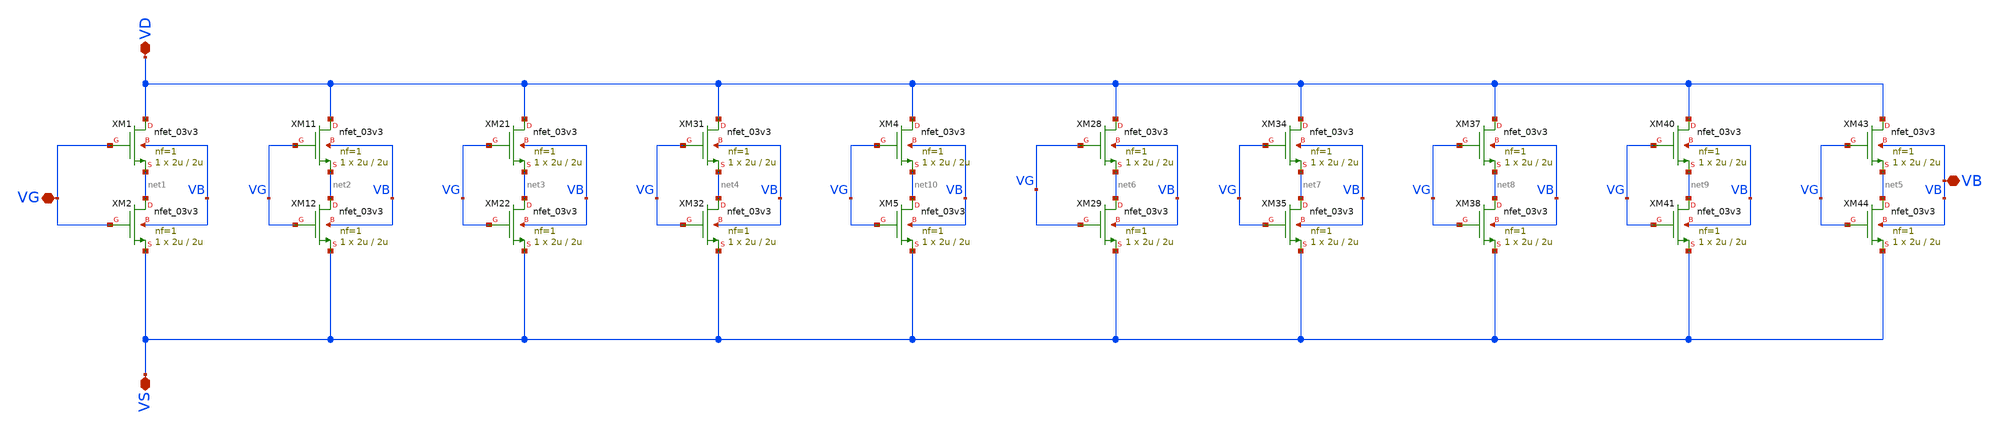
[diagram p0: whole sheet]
** sch_path: Voltage_Reference/symbols_vr/NMOS_association_10u_6u_V2.sch
**.subckt NMOS_association_10u_6u_V2 VD VB VG VS
*.iopin VD
*.iopin VB
*.iopin VG
*.iopin VS
XM1 VD VG net1 VB nfet_03v3 L=2u W=2u nf=1 ad='int((nf+1)/2) * W/nf * 0.18u' as='int((nf+2)/2) * W/nf * 0.18u'
+ pd='2*int((nf+1)/2) * (W/nf + 0.18u)' ps='2*int((nf+2)/2) * (W/nf + 0.18u)' nrd='0.18u / W' nrs='0.18u / W'
+ sa=0 sb=0 sd=0 m=1
XM2 net1 VG VS VB nfet_03v3 L=2u W=2u nf=1 ad='int((nf+1)/2) * W/nf * 0.18u' as='int((nf+2)/2) * W/nf * 0.18u'
+ pd='2*int((nf+1)/2) * (W/nf + 0.18u)' ps='2*int((nf+2)/2) * (W/nf + 0.18u)' nrd='0.18u / W' nrs='0.18u / W'
+ sa=0 sb=0 sd=0 m=1
XM11 VD VG net2 VB nfet_03v3 L=2u W=2u nf=1 ad='int((nf+1)/2) * W/nf * 0.18u' as='int((nf+2)/2) * W/nf * 0.18u'
+ pd='2*int((nf+1)/2) * (W/nf + 0.18u)' ps='2*int((nf+2)/2) * (W/nf + 0.18u)' nrd='0.18u / W' nrs='0.18u / W'
+ sa=0 sb=0 sd=0 m=1
XM12 net2 VG VS VB nfet_03v3 L=2u W=2u nf=1 ad='int((nf+1)/2) * W/nf * 0.18u' as='int((nf+2)/2) * W/nf * 0.18u'
+ pd='2*int((nf+1)/2) * (W/nf + 0.18u)' ps='2*int((nf+2)/2) * (W/nf + 0.18u)' nrd='0.18u / W' nrs='0.18u / W'
+ sa=0 sb=0 sd=0 m=1
XM21 VD VG net3 VB nfet_03v3 L=2u W=2u nf=1 ad='int((nf+1)/2) * W/nf * 0.18u' as='int((nf+2)/2) * W/nf * 0.18u'
+ pd='2*int((nf+1)/2) * (W/nf + 0.18u)' ps='2*int((nf+2)/2) * (W/nf + 0.18u)' nrd='0.18u / W' nrs='0.18u / W'
+ sa=0 sb=0 sd=0 m=1
XM22 net3 VG VS VB nfet_03v3 L=2u W=2u nf=1 ad='int((nf+1)/2) * W/nf * 0.18u' as='int((nf+2)/2) * W/nf * 0.18u'
+ pd='2*int((nf+1)/2) * (W/nf + 0.18u)' ps='2*int((nf+2)/2) * (W/nf + 0.18u)' nrd='0.18u / W' nrs='0.18u / W'
+ sa=0 sb=0 sd=0 m=1
XM31 VD VG net4 VB nfet_03v3 L=2u W=2u nf=1 ad='int((nf+1)/2) * W/nf * 0.18u' as='int((nf+2)/2) * W/nf * 0.18u'
+ pd='2*int((nf+1)/2) * (W/nf + 0.18u)' ps='2*int((nf+2)/2) * (W/nf + 0.18u)' nrd='0.18u / W' nrs='0.18u / W'
+ sa=0 sb=0 sd=0 m=1
XM32 net4 VG VS VB nfet_03v3 L=2u W=2u nf=1 ad='int((nf+1)/2) * W/nf * 0.18u' as='int((nf+2)/2) * W/nf * 0.18u'
+ pd='2*int((nf+1)/2) * (W/nf + 0.18u)' ps='2*int((nf+2)/2) * (W/nf + 0.18u)' nrd='0.18u / W' nrs='0.18u / W'
+ sa=0 sb=0 sd=0 m=1
XM4 VD VG net10 VB nfet_03v3 L=2u W=2u nf=1 ad='int((nf+1)/2) * W/nf * 0.18u' as='int((nf+2)/2) * W/nf * 0.18u'
+ pd='2*int((nf+1)/2) * (W/nf + 0.18u)' ps='2*int((nf+2)/2) * (W/nf + 0.18u)' nrd='0.18u / W' nrs='0.18u / W'
+ sa=0 sb=0 sd=0 m=1
XM5 net10 VG VS VB nfet_03v3 L=2u W=2u nf=1 ad='int((nf+1)/2) * W/nf * 0.18u' as='int((nf+2)/2) * W/nf * 0.18u'
+ pd='2*int((nf+1)/2) * (W/nf + 0.18u)' ps='2*int((nf+2)/2) * (W/nf + 0.18u)' nrd='0.18u / W' nrs='0.18u / W'
+ sa=0 sb=0 sd=0 m=1
XM28 VD VG net6 VB nfet_03v3 L=2u W=2u nf=1 ad='int((nf+1)/2) * W/nf * 0.18u' as='int((nf+2)/2) * W/nf * 0.18u'
+ pd='2*int((nf+1)/2) * (W/nf + 0.18u)' ps='2*int((nf+2)/2) * (W/nf + 0.18u)' nrd='0.18u / W' nrs='0.18u / W'
+ sa=0 sb=0 sd=0 m=1
XM29 net6 VG VS VB nfet_03v3 L=2u W=2u nf=1 ad='int((nf+1)/2) * W/nf * 0.18u' as='int((nf+2)/2) * W/nf * 0.18u'
+ pd='2*int((nf+1)/2) * (W/nf + 0.18u)' ps='2*int((nf+2)/2) * (W/nf + 0.18u)' nrd='0.18u / W' nrs='0.18u / W'
+ sa=0 sb=0 sd=0 m=1
XM34 VD VG net7 VB nfet_03v3 L=2u W=2u nf=1 ad='int((nf+1)/2) * W/nf * 0.18u' as='int((nf+2)/2) * W/nf * 0.18u'
+ pd='2*int((nf+1)/2) * (W/nf + 0.18u)' ps='2*int((nf+2)/2) * (W/nf + 0.18u)' nrd='0.18u / W' nrs='0.18u / W'
+ sa=0 sb=0 sd=0 m=1
XM35 net7 VG VS VB nfet_03v3 L=2u W=2u nf=1 ad='int((nf+1)/2) * W/nf * 0.18u' as='int((nf+2)/2) * W/nf * 0.18u'
+ pd='2*int((nf+1)/2) * (W/nf + 0.18u)' ps='2*int((nf+2)/2) * (W/nf + 0.18u)' nrd='0.18u / W' nrs='0.18u / W'
+ sa=0 sb=0 sd=0 m=1
XM37 VD VG net8 VB nfet_03v3 L=2u W=2u nf=1 ad='int((nf+1)/2) * W/nf * 0.18u' as='int((nf+2)/2) * W/nf * 0.18u'
+ pd='2*int((nf+1)/2) * (W/nf + 0.18u)' ps='2*int((nf+2)/2) * (W/nf + 0.18u)' nrd='0.18u / W' nrs='0.18u / W'
+ sa=0 sb=0 sd=0 m=1
XM38 net8 VG VS VB nfet_03v3 L=2u W=2u nf=1 ad='int((nf+1)/2) * W/nf * 0.18u' as='int((nf+2)/2) * W/nf * 0.18u'
+ pd='2*int((nf+1)/2) * (W/nf + 0.18u)' ps='2*int((nf+2)/2) * (W/nf + 0.18u)' nrd='0.18u / W' nrs='0.18u / W'
+ sa=0 sb=0 sd=0 m=1
XM40 VD VG net9 VB nfet_03v3 L=2u W=2u nf=1 ad='int((nf+1)/2) * W/nf * 0.18u' as='int((nf+2)/2) * W/nf * 0.18u'
+ pd='2*int((nf+1)/2) * (W/nf + 0.18u)' ps='2*int((nf+2)/2) * (W/nf + 0.18u)' nrd='0.18u / W' nrs='0.18u / W'
+ sa=0 sb=0 sd=0 m=1
XM41 net9 VG VS VB nfet_03v3 L=2u W=2u nf=1 ad='int((nf+1)/2) * W/nf * 0.18u' as='int((nf+2)/2) * W/nf * 0.18u'
+ pd='2*int((nf+1)/2) * (W/nf + 0.18u)' ps='2*int((nf+2)/2) * (W/nf + 0.18u)' nrd='0.18u / W' nrs='0.18u / W'
+ sa=0 sb=0 sd=0 m=1
XM43 VD VG net5 VB nfet_03v3 L=2u W=2u nf=1 ad='int((nf+1)/2) * W/nf * 0.18u' as='int((nf+2)/2) * W/nf * 0.18u'
+ pd='2*int((nf+1)/2) * (W/nf + 0.18u)' ps='2*int((nf+2)/2) * (W/nf + 0.18u)' nrd='0.18u / W' nrs='0.18u / W'
+ sa=0 sb=0 sd=0 m=1
XM44 net5 VG VS VB nfet_03v3 L=2u W=2u nf=1 ad='int((nf+1)/2) * W/nf * 0.18u' as='int((nf+2)/2) * W/nf * 0.18u'
+ pd='2*int((nf+1)/2) * (W/nf + 0.18u)' ps='2*int((nf+2)/2) * (W/nf + 0.18u)' nrd='0.18u / W' nrs='0.18u / W'
+ sa=0 sb=0 sd=0 m=1
**.ends
.end
